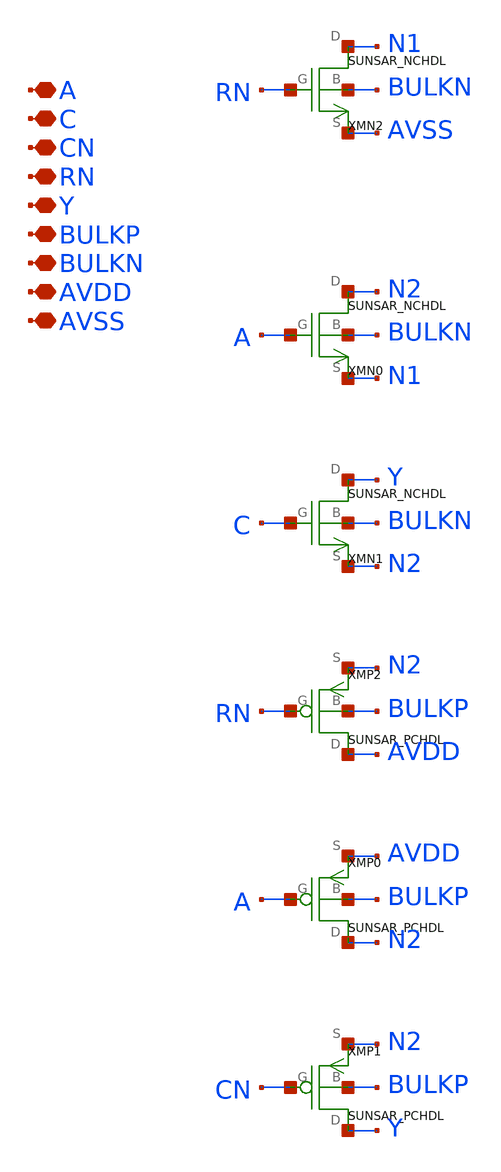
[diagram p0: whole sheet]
** sch_path: design/SUN_SAR9B_SKY130NM/SUNSAR_NDTRIX1_CV.sch
**.subckt SUNSAR_NDTRIX1_CV A C CN RN Y BULKP BULKN AVDD AVSS
*.iopin A
*.iopin C
*.iopin CN
*.iopin RN
*.iopin Y
*.iopin BULKP
*.iopin BULKN
*.iopin AVDD
*.iopin AVSS
XMN2 N1 RN AVSS BULKN SUNSAR_NCHDL
XMN0 N2 A N1 BULKN SUNSAR_NCHDL
XMN1 Y C N2 BULKN SUNSAR_NCHDL
XMP2 AVDD RN N2 BULKP SUNSAR_PCHDL
XMP0 N2 A AVDD BULKP SUNSAR_PCHDL
XMP1 Y CN N2 BULKP SUNSAR_PCHDL
**.ends
.end
